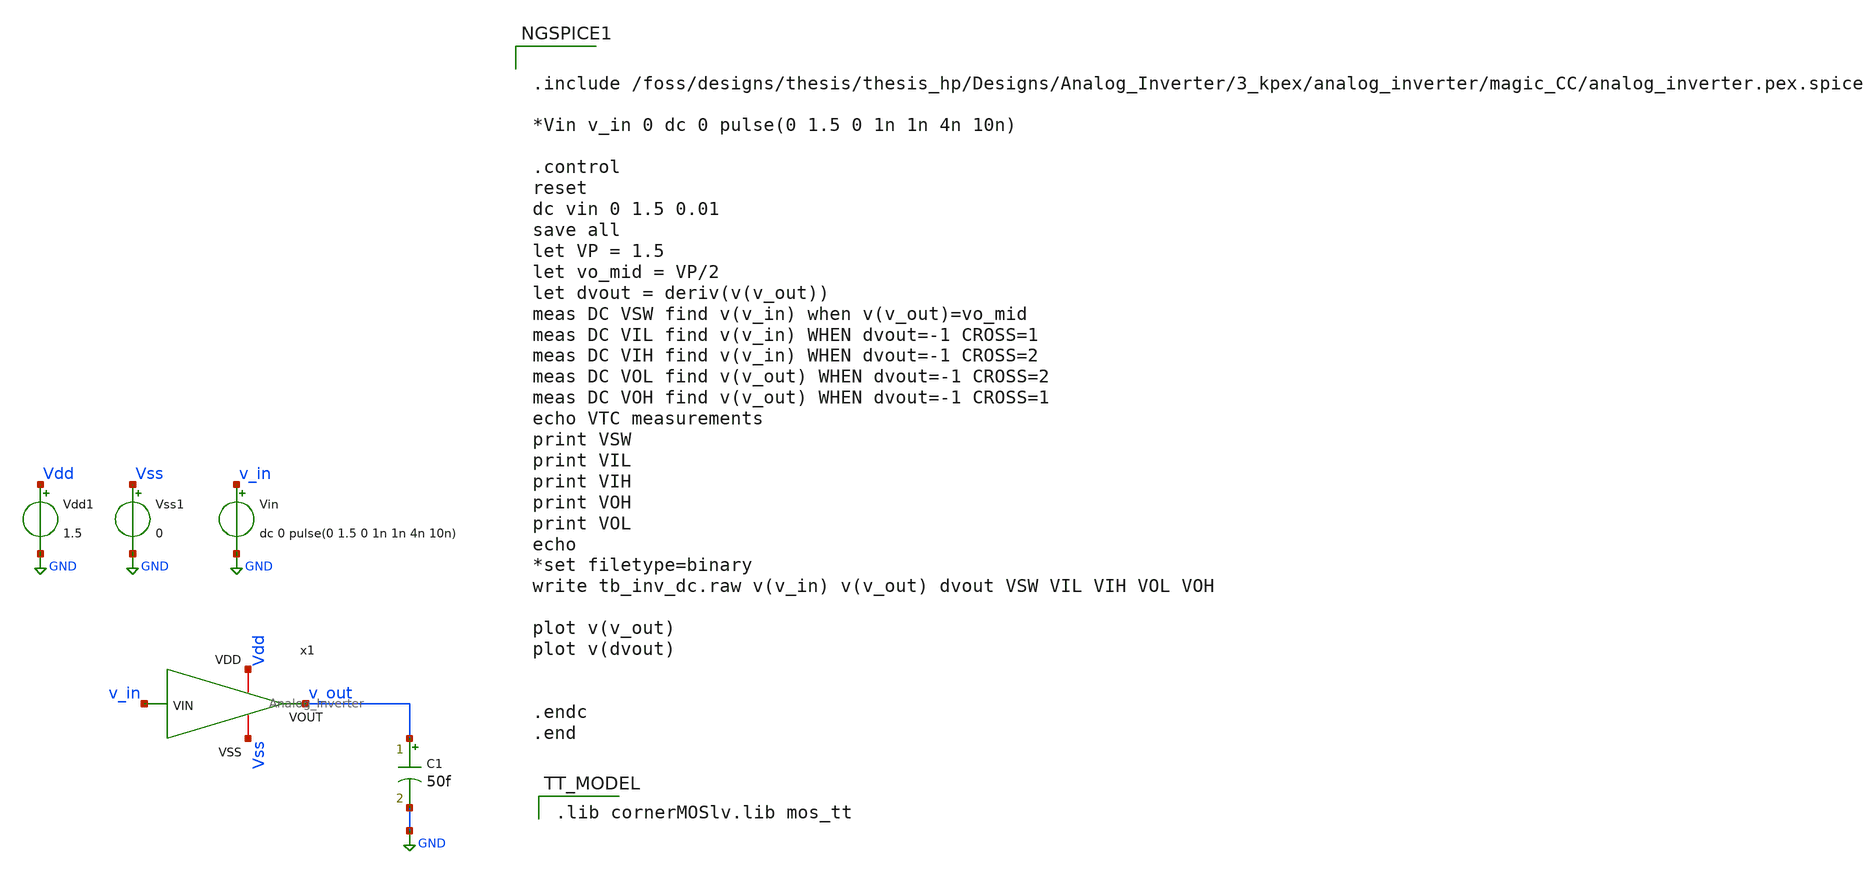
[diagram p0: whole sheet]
** sch_path: files/Analog_Inverter/1_schematics/tb_Analog_Inverter_dc.sch
* (c) 2024 Hrishikesh, @HSB
**.subckt tb_Analog_Inverter_dc
Vdd1 Vdd GND 1.5
Vss1 Vss GND 0
Vin v_in GND dc 0 pulse(0 1.5 0 1n 1n 4n 10n)
C1 v_out GND 50f m=1
x1 Vdd v_in v_out Vss Analog_Inverter
**** begin user architecture code


.include /foss/designs/thesis/thesis_hp/Designs/Analog_Inverter/3_kpex/analog_inverter/magic_CC/analog_inverter.pex.spice

*Vin v_in 0 dc 0 pulse(0 1.5 0 1n 1n 4n 10n)

.control
reset
dc vin 0 1.5 0.01
save all
let VP = 1.5
let vo_mid = VP/2
let dvout = deriv(v(v_out))
meas DC VSW find v(v_in) when v(v_out)=vo_mid
meas DC VIL find v(v_in) WHEN dvout=-1 CROSS=1
meas DC VIH find v(v_in) WHEN dvout=-1 CROSS=2
meas DC VOL find v(v_out) WHEN dvout=-1 CROSS=2
meas DC VOH find v(v_out) WHEN dvout=-1 CROSS=1
echo VTC measurements
print VSW
print VIL
print VIH
print VOH
print VOL
echo
*set filetype=binary
write tb_inv_dc.raw v(v_in) v(v_out) dvout VSW VIL VIH VOL VOH

plot v(v_out)
plot v(dvout)


.endc
.end


 .lib cornerMOSlv.lib mos_tt

**** end user architecture code
**.ends
.GLOBAL GND
.end
